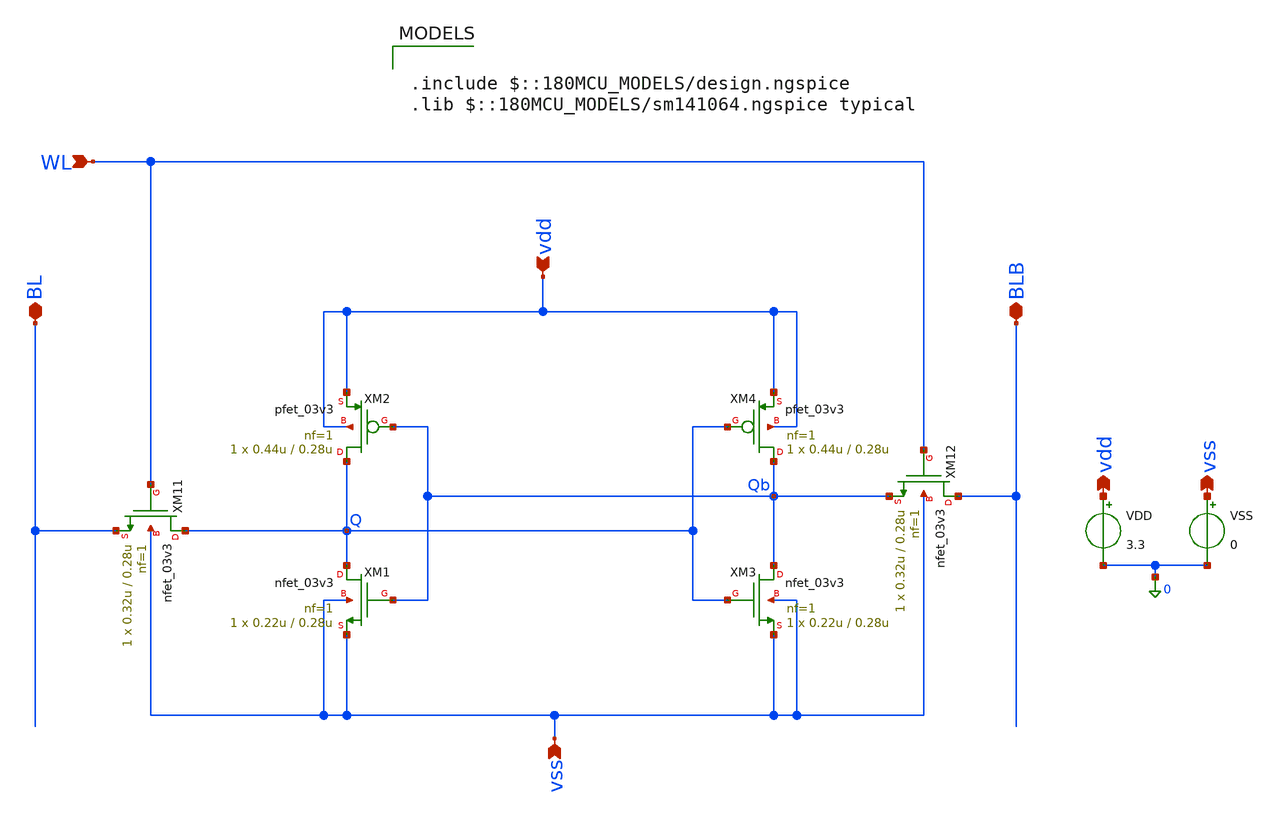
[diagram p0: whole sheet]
** sch_path: analog/tests/6t_sram_03v3_write_snm_tb.sch
**.subckt 6t_sram_03v3_write_snm_tb vdd vss BL WL BLB vss vdd
*.ipin vdd
*.ipin vss
*.iopin BL
*.ipin WL
*.iopin BLB
*.opin vss
*.opin vdd
XM1 Q Qb vss vss nfet_03v3 L=0.28u W=0.22u nf=1 ad='int((nf+1)/2) * W/nf * 0.18u' as='int((nf+2)/2) * W/nf * 0.18u'
+ pd='2*int((nf+1)/2) * (W/nf + 0.18u)' ps='2*int((nf+2)/2) * (W/nf + 0.18u)' nrd='0.18u / W' nrs='0.18u / W'
+ sa=0 sb=0 sd=0 m=1
XM2 Q Qb vdd vdd pfet_03v3 L=0.28u W=0.44u nf=1 ad='int((nf+1)/2) * W/nf * 0.18u' as='int((nf+2)/2) * W/nf * 0.18u'
+ pd='2*int((nf+1)/2) * (W/nf + 0.18u)' ps='2*int((nf+2)/2) * (W/nf + 0.18u)' nrd='0.18u / W' nrs='0.18u / W'
+ sa=0 sb=0 sd=0 m=1
XM3 Qb Q vss vss nfet_03v3 L=0.28u W=0.22u nf=1 ad='int((nf+1)/2) * W/nf * 0.18u' as='int((nf+2)/2) * W/nf * 0.18u'
+ pd='2*int((nf+1)/2) * (W/nf + 0.18u)' ps='2*int((nf+2)/2) * (W/nf + 0.18u)' nrd='0.18u / W' nrs='0.18u / W'
+ sa=0 sb=0 sd=0 m=1
XM4 Qb Q vdd vdd pfet_03v3 L=0.28u W=0.44u nf=1 ad='int((nf+1)/2) * W/nf * 0.18u' as='int((nf+2)/2) * W/nf * 0.18u'
+ pd='2*int((nf+1)/2) * (W/nf + 0.18u)' ps='2*int((nf+2)/2) * (W/nf + 0.18u)' nrd='0.18u / W' nrs='0.18u / W'
+ sa=0 sb=0 sd=0 m=1
XM11 Q WL BL vss nfet_03v3 L=0.28u W=0.32u nf=1 ad='int((nf+1)/2) * W/nf * 0.18u' as='int((nf+2)/2) * W/nf * 0.18u'
+ pd='2*int((nf+1)/2) * (W/nf + 0.18u)' ps='2*int((nf+2)/2) * (W/nf + 0.18u)' nrd='0.18u / W' nrs='0.18u / W'
+ sa=0 sb=0 sd=0 m=1
XM12 BLB WL Qb vss nfet_03v3 L=0.28u W=0.32u nf=1 ad='int((nf+1)/2) * W/nf * 0.18u' as='int((nf+2)/2) * W/nf * 0.18u'
+ pd='2*int((nf+1)/2) * (W/nf + 0.18u)' ps='2*int((nf+2)/2) * (W/nf + 0.18u)' nrd='0.18u / W' nrs='0.18u / W'
+ sa=0 sb=0 sd=0 m=1
VDD vdd 0 3.3
VSS vss 0 0
**** begin user architecture code

.include $::180MCU_MODELS/design.ngspice
.lib $::180MCU_MODELS/sm141064.ngspice typical



** Parameters
.param V1=0
.param Td=2n
.param Tr=0.1n
.param Tf=0.1n
.param PW=3n
.param PER=50n
.param NP=1

** Sources
VBLB BLB 0 DC 3.3
VBL BL 0 DC 0
VWL WL 0 PULSE({V1} 3.3 {Td} {Tr} {Tf} {PW} {PER} {NP})
** Initial States
.ic v(Q)=3.3 v(Qb)=0
** Control Section Params
.csparam V_H=3.3
.csparam V_L=0
.csparam V1={V1}
.csparam Td={Td}
.csparam Tr={Tr}
.csparam Tf={Tf}
.csparam PW={PW}
.csparam PER={PER}
.csparam NP={NP}
.csparam tran_time=0.1u

.control
save all

** Initial Conditions
ic v(Q)=3.3 v(Qb)=0

** Word-Line Write Margin
let WL_H = V_H
let WL_L = V_L
let max_err  = 0.01
let v_trip = V_H/2
*****************
* Initial tests *
*****************
** Test Flip at WL=VDD
let flip_b = 0
alter @vwl[pulse] = [ $&V1 $&V_H &Td $&Tr $&Tf $&PW $&PER $&NP ]

tran 0.1n $&tran_time uic

let final_q = v(Q)[length(v(Q))-1]
if final_q le v_trip
	let flip_b = 1
	echo Init_Test 1/2 [PASS] Flipped @ WL=VDD
	echo
else
	let flip_b = 0
	echo Init_Test 1/2 [FAIL] Not Flipped @ WL=VDD
	echo
end

*** Test No-Flip at WL=0
let noflip_b = 0

alter @vwl[pulse] = [ $&V1 $&V_L $&Td $&Tr $&Tf $&PW $&PER $&NP ]

tran 0.1n $&tran_time uic

let final_q = v(Q)[length(v(Q))-1]
if final_q le v_trip
	let noflip_b = 0
	echo Init_Test 2/2 [FAIL] Flipped @ WL=0
	echo
else
	let noflip_b = 1
	echo Init_Test 2/2 [PASS] Not Flipped @ WL=0
	echo
end
************************
* Assert Initial Tests *
************************
let bool_b = flip_b * noflip_b	; Set Boolean for algo if case
if bool_b = 0
  echo Initial Tests Failed, Check Schematic and .ic
else
  setplot const
  echo Initial Tests PASSED!
  echo Performing Word-Line Write Voltage Margin Bisection Algorithm
  echo

let WL_H = V_H
let WL_L = V_L
let max_err  = 0.01
let v_trip = V_H/2

  let WL_m = 0
  while WL_H-WL_L > max_err
  let WL_m = (WL_H + WL_L)/2
  alter @vwl[pulse] = [ 0 $&WL_m $&Td $&Tr $&Tf $&PW $&PER $&NP ]
  echo Rise Parameter $&WL_m
  print @vwl[pulse][1]
  echo
  tran 0.1n $&tran_time uic
  * Print Q & Qb
  echo Initial States
  print v(Q)[15] v(Qb)[15]
  echo Final States
  print v(Q)[length(v(Q))-1] v(Qb)[length(v(Qb))-1]
  echo
  let final_q = v(Q)[length(v(Q))-1]

  if final_q < v_trip
	let WL_H = WL_m
	echo WL_mid = $&WL_m Flipped
  else
	if final_q > v_trip
		let WL_L = WL_m
		echo WL_mid =  $&WL_m Not Flipped
	else
		let margin = V_H - WL_H
		echo Word-Trip Voltage Margin Found: $&margin
		.plot v(WL)
	end
  end
  let diff = WL_H-WL_L
  print WL_H WL_L
  echo difference= $&diff
  echo
  end
let margin = V_H - WL_H
echo margin= $&margin
end
write 6t_sram_03v3_snm_tb.raw
.endc
.end


**** end user architecture code
**.ends
.end
